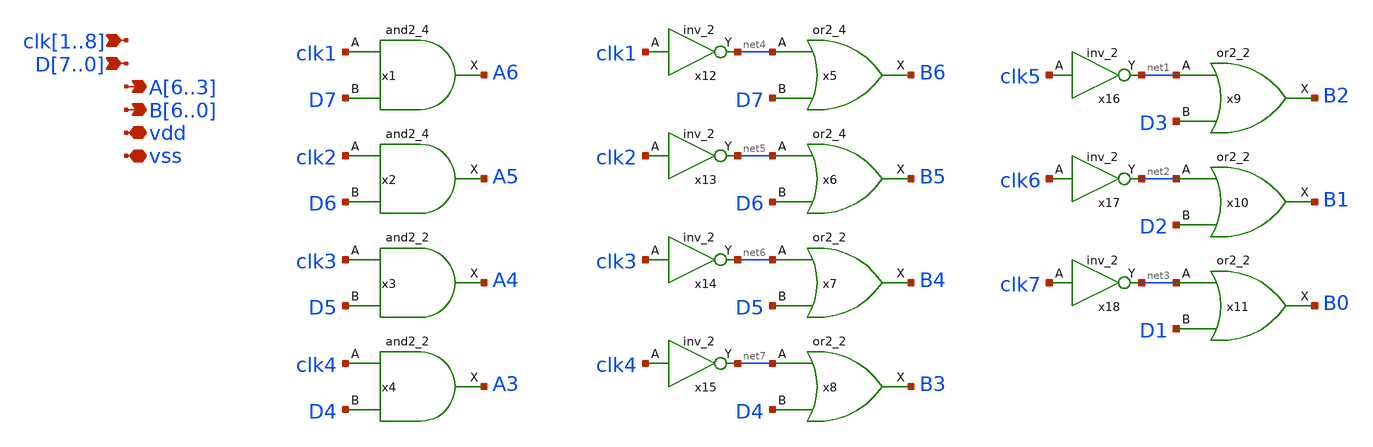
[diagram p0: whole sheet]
** sch_path: xschem/sar-adc/cdac_driver.sch
**.subckt cdac_driver D7,D6,D5,D4,D3,D2,D1,D0 A6,A5,A4,A3 B6,B5,B4,B3,B2,B1,B0 vdd vss
*+ clk1,clk2,clk3,clk4,clk5,clk6,clk7,clk8
*.ipin D7,D6,D5,D4,D3,D2,D1,D0
*.opin A6,A5,A4,A3
*.opin B6,B5,B4,B3,B2,B1,B0
*.iopin vdd
*.iopin vss
*.ipin clk1,clk2,clk3,clk4,clk5,clk6,clk7,clk8
x7 net6 D5 vss vss vdd vdd B4 sky130_fd_sc_hd__or2_2
x8 net7 D4 vss vss vdd vdd B3 sky130_fd_sc_hd__or2_2
x9 net1 D3 vss vss vdd vdd B2 sky130_fd_sc_hd__or2_2
x10 net2 D2 vss vss vdd vdd B1 sky130_fd_sc_hd__or2_2
x11 net3 D1 vss vss vdd vdd B0 sky130_fd_sc_hd__or2_2
x3 clk3 D5 vss vss vdd vdd A4 sky130_fd_sc_hd__and2_2
x4 clk4 D4 vss vss vdd vdd A3 sky130_fd_sc_hd__and2_2
x12 clk1 vss vss vdd vdd net4 sky130_fd_sc_hd__inv_2
x13 clk2 vss vss vdd vdd net5 sky130_fd_sc_hd__inv_2
x14 clk3 vss vss vdd vdd net6 sky130_fd_sc_hd__inv_2
x15 clk4 vss vss vdd vdd net7 sky130_fd_sc_hd__inv_2
x16 clk5 vss vss vdd vdd net1 sky130_fd_sc_hd__inv_2
x17 clk6 vss vss vdd vdd net2 sky130_fd_sc_hd__inv_2
x18 clk7 vss vss vdd vdd net3 sky130_fd_sc_hd__inv_2
x1 clk1 D7 vss vss vdd vdd A6 sky130_fd_sc_hd__and2_4
x2 clk2 D6 vss vss vdd vdd A5 sky130_fd_sc_hd__and2_4
x5 net4 D7 vss vss vdd vdd B6 sky130_fd_sc_hd__or2_4
x6 net5 D6 vss vss vdd vdd B5 sky130_fd_sc_hd__or2_4
**.ends
.end
